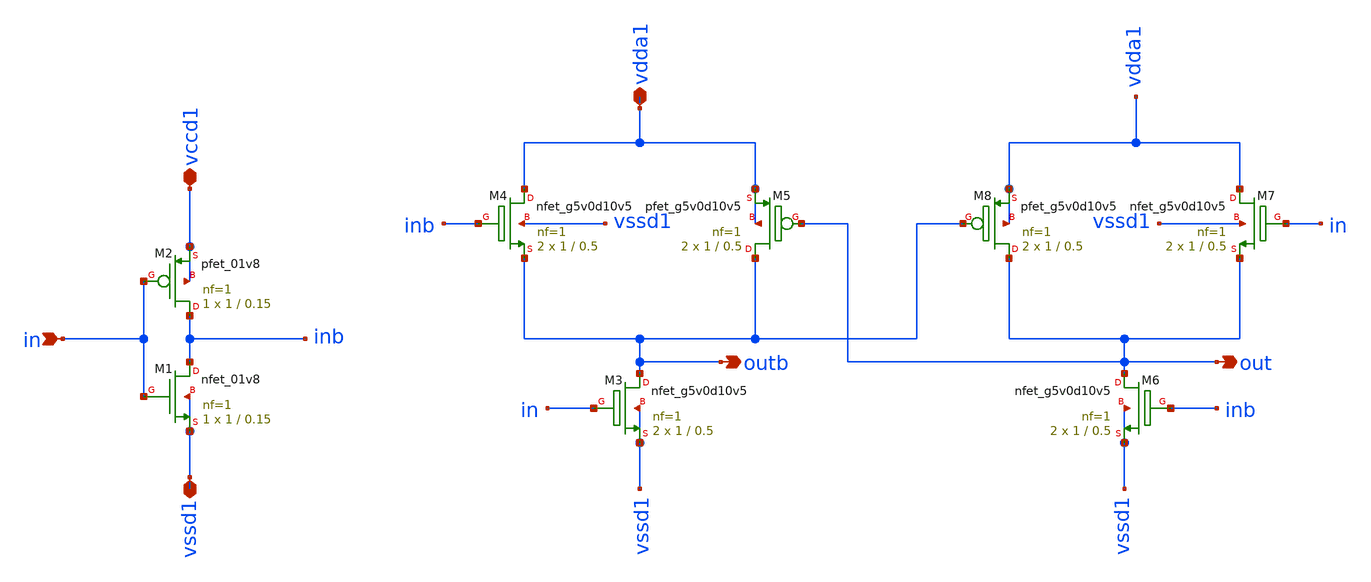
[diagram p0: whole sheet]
** sch_path: xschem/level_up_shifter_2x.sch
**.subckt level_up_shifter_2x in vccd1 vssd1 vdda1 out outb
*.ipin in
*.iopin vccd1
*.iopin vssd1
*.iopin vdda1
*.opin out
*.opin outb
XM1 inb in vssd1 vssd1 sky130_fd_pr__nfet_01v8 L=0.15 W=1 nf=1 ad='int((nf+1)/2) * W/nf * 0.29' as='int((nf+2)/2) * W/nf * 0.29'
+ pd='2*int((nf+1)/2) * (W/nf + 0.29)' ps='2*int((nf+2)/2) * (W/nf + 0.29)' nrd='0.29 / W' nrs='0.29 / W'
+ sa=0 sb=0 sd=0 mult=1 m=1
XM2 inb in vccd1 vccd1 sky130_fd_pr__pfet_01v8 L=0.15 W=1 nf=1 ad='int((nf+1)/2) * W/nf * 0.29' as='int((nf+2)/2) * W/nf * 0.29'
+ pd='2*int((nf+1)/2) * (W/nf + 0.29)' ps='2*int((nf+2)/2) * (W/nf + 0.29)' nrd='0.29 / W' nrs='0.29 / W'
+ sa=0 sb=0 sd=0 mult=1 m=1
XM3 outb in vssd1 vssd1 sky130_fd_pr__nfet_g5v0d10v5 L=0.5 W=1 nf=1 ad='int((nf+1)/2) * W/nf * 0.29'
+ as='int((nf+2)/2) * W/nf * 0.29' pd='2*int((nf+1)/2) * (W/nf + 0.29)' ps='2*int((nf+2)/2) * (W/nf + 0.29)'
+ nrd='0.29 / W' nrs='0.29 / W' sa=0 sb=0 sd=0 mult=2 m=2
XM4 vdda1 inb outb vssd1 sky130_fd_pr__nfet_g5v0d10v5 L=0.5 W=1 nf=1 ad='int((nf+1)/2) * W/nf * 0.29'
+ as='int((nf+2)/2) * W/nf * 0.29' pd='2*int((nf+1)/2) * (W/nf + 0.29)' ps='2*int((nf+2)/2) * (W/nf + 0.29)'
+ nrd='0.29 / W' nrs='0.29 / W' sa=0 sb=0 sd=0 mult=2 m=2
XM5 outb out vdda1 vdda1 sky130_fd_pr__pfet_g5v0d10v5 L=0.5 W=1 nf=1 ad='int((nf+1)/2) * W/nf * 0.29'
+ as='int((nf+2)/2) * W/nf * 0.29' pd='2*int((nf+1)/2) * (W/nf + 0.29)' ps='2*int((nf+2)/2) * (W/nf + 0.29)'
+ nrd='0.29 / W' nrs='0.29 / W' sa=0 sb=0 sd=0 mult=2 m=2
XM6 out inb vssd1 vssd1 sky130_fd_pr__nfet_g5v0d10v5 L=0.5 W=1 nf=1 ad='int((nf+1)/2) * W/nf * 0.29'
+ as='int((nf+2)/2) * W/nf * 0.29' pd='2*int((nf+1)/2) * (W/nf + 0.29)' ps='2*int((nf+2)/2) * (W/nf + 0.29)'
+ nrd='0.29 / W' nrs='0.29 / W' sa=0 sb=0 sd=0 mult=2 m=2
XM7 vdda1 in out vssd1 sky130_fd_pr__nfet_g5v0d10v5 L=0.5 W=1 nf=1 ad='int((nf+1)/2) * W/nf * 0.29' as='int((nf+2)/2) * W/nf * 0.29'
+ pd='2*int((nf+1)/2) * (W/nf + 0.29)' ps='2*int((nf+2)/2) * (W/nf + 0.29)' nrd='0.29 / W' nrs='0.29 / W'
+ sa=0 sb=0 sd=0 mult=2 m=2
XM8 out outb vdda1 vdda1 sky130_fd_pr__pfet_g5v0d10v5 L=0.5 W=1 nf=1 ad='int((nf+1)/2) * W/nf * 0.29'
+ as='int((nf+2)/2) * W/nf * 0.29' pd='2*int((nf+1)/2) * (W/nf + 0.29)' ps='2*int((nf+2)/2) * (W/nf + 0.29)'
+ nrd='0.29 / W' nrs='0.29 / W' sa=0 sb=0 sd=0 mult=2 m=2
**.ends
.end
